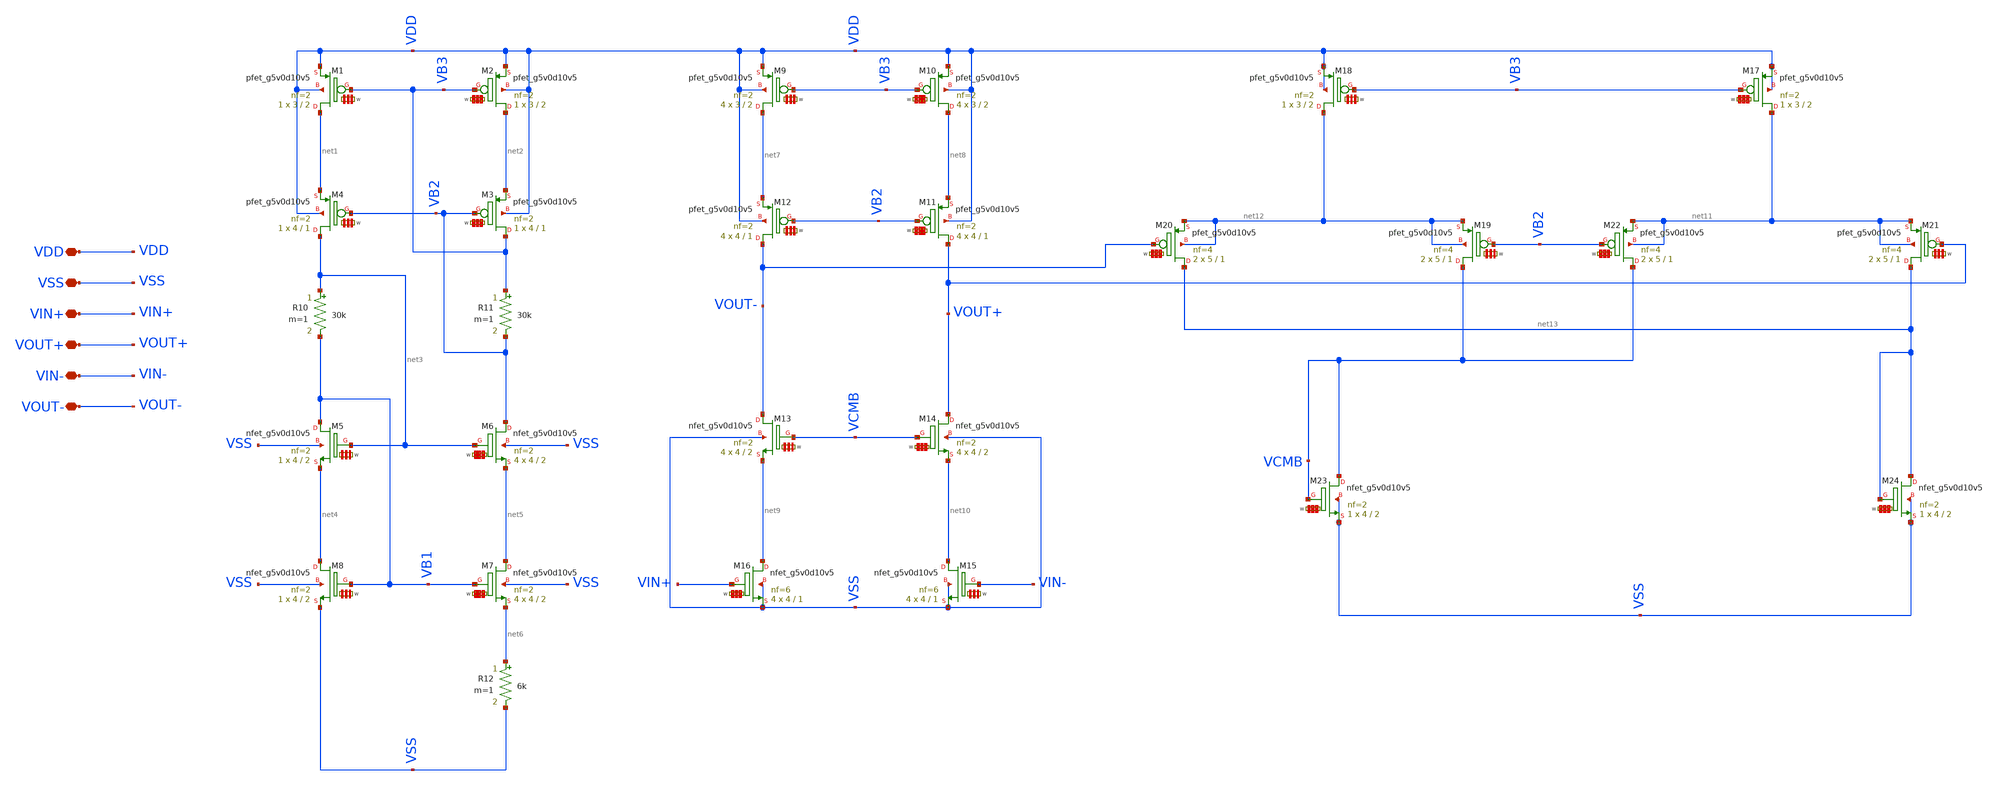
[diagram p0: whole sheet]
** sch_path: my_ip/sky130A/fully_differential_telescopic_cascode_5V_V1/fd_opamp.sch
**.subckt fd_opamp VDD VSS VIN+ VOUT+ VIN- VOUT-
*.iopin VDD
*.iopin VSS
*.iopin VIN+
*.iopin VOUT+
*.iopin VIN-
*.iopin VOUT-
XM1 net1 VB3 VDD VDD sky130_fd_pr__pfet_g5v0d10v5 L=2 W='3 * 2 ' nf=2 ad='int((2 + 1)/2) * 3 * 0.29'
+ as='int((2 + 2)/2) * 3 * 0.29' pd='2*int((2 + 1)/2) * (3 + 0.29)' ps='2*int((2 + 2)/2) * (3 + 0.29)'
+ nrd='0.29 / 3 / 2 ' nrs='0.29 / 3 / 2 ' sa=0 sb=0 sd=0 mult=1 m=1
XM3 VB3 VB2 net2 VDD sky130_fd_pr__pfet_g5v0d10v5 L=1 W='4 * 2 ' nf=2 ad='int((2 + 1)/2) * 4 * 0.29'
+ as='int((2 + 2)/2) * 4 * 0.29' pd='2*int((2 + 1)/2) * (4 + 0.29)' ps='2*int((2 + 2)/2) * (4 + 0.29)'
+ nrd='0.29 / 4 / 2 ' nrs='0.29 / 4 / 2 ' sa=0 sb=0 sd=0 mult=1 m=1
R10 net3 VB1 30k m=1
R11 VB3 VB2 30k m=1
XM7 net5 VB1 net6 VSS sky130_fd_pr__nfet_g5v0d10v5 L=2 W='4 * 2 ' nf=2 ad='int((nf+1)/2) * W / nf * 0.29'
+ as='int((nf+2)/2) * W / nf * 0.29' pd='2*int((nf+1)/2) * (W / nf + 0.29)' ps='2*int((nf+2)/2) * (W / nf + 0.29)'
+ nrd='0.29 / W ' nrs='0.29 / W ' sa=0 sb=0 sd=0 mult=4 m=4
R12 net6 VSS 6k m=1
XM2 net2 VB3 VDD VDD sky130_fd_pr__pfet_g5v0d10v5 L=2 W='3 * 2 ' nf=2 ad='int((2 + 1)/2) * 3 * 0.29'
+ as='int((2 + 2)/2) * 3 * 0.29' pd='2*int((2 + 1)/2) * (3 + 0.29)' ps='2*int((2 + 2)/2) * (3 + 0.29)'
+ nrd='0.29 / 3 / 2 ' nrs='0.29 / 3 / 2 ' sa=0 sb=0 sd=0 mult=1 m=1
XM6 VB2 net3 net5 VSS sky130_fd_pr__nfet_g5v0d10v5 L=2 W='4 * 2 ' nf=2 ad='int((nf+1)/2) * W / nf * 0.29'
+ as='int((nf+2)/2) * W / nf * 0.29' pd='2*int((nf+1)/2) * (W / nf + 0.29)' ps='2*int((nf+2)/2) * (W / nf + 0.29)'
+ nrd='0.29 / W ' nrs='0.29 / W ' sa=0 sb=0 sd=0 mult=4 m=4
XM5 VB1 net3 net4 VSS sky130_fd_pr__nfet_g5v0d10v5 L=2 W='4 * 2 ' nf=2 ad='int((nf+1)/2) * W / nf * 0.29'
+ as='int((nf+2)/2) * W / nf * 0.29' pd='2*int((nf+1)/2) * (W / nf + 0.29)' ps='2*int((nf+2)/2) * (W / nf + 0.29)'
+ nrd='0.29 / W ' nrs='0.29 / W ' sa=0 sb=0 sd=0 mult=1 m=1
XM8 net4 VB1 VSS VSS sky130_fd_pr__nfet_g5v0d10v5 L=2 W='4 * 2 ' nf=2 ad='int((nf+1)/2) * W / nf * 0.29'
+ as='int((nf+2)/2) * W / nf * 0.29' pd='2*int((nf+1)/2) * (W / nf + 0.29)' ps='2*int((nf+2)/2) * (W / nf + 0.29)'
+ nrd='0.29 / W ' nrs='0.29 / W ' sa=0 sb=0 sd=0 mult=1 m=1
XM4 net3 VB2 net1 VDD sky130_fd_pr__pfet_g5v0d10v5 L=1 W='4 * 2 ' nf=2 ad='int((2 + 1)/2) * 4 * 0.29'
+ as='int((2 + 2)/2) * 4 * 0.29' pd='2*int((2 + 1)/2) * (4 + 0.29)' ps='2*int((2 + 2)/2) * (4 + 0.29)'
+ nrd='0.29 / 4 / 2 ' nrs='0.29 / 4 / 2 ' sa=0 sb=0 sd=0 mult=1 m=1
XM9 net7 VB3 VDD VDD sky130_fd_pr__pfet_g5v0d10v5 L=2 W='3 * 2 ' nf=2 ad='int((2 + 1)/2) * 3 * 0.29'
+ as='int((2 + 2)/2) * 3 * 0.29' pd='2*int((2 + 1)/2) * (3 + 0.29)' ps='2*int((2 + 2)/2) * (3 + 0.29)'
+ nrd='0.29 / 3 / 2 ' nrs='0.29 / 3 / 2 ' sa=0 sb=0 sd=0 mult=4 m=4
XM10 net8 VB3 VDD VDD sky130_fd_pr__pfet_g5v0d10v5 L=2 W='3 * 2 ' nf=2 ad='int((2 + 1)/2) * 3 * 0.29'
+ as='int((2 + 2)/2) * 3 * 0.29' pd='2*int((2 + 1)/2) * (3 + 0.29)' ps='2*int((2 + 2)/2) * (3 + 0.29)'
+ nrd='0.29 / 3 / 2 ' nrs='0.29 / 3 / 2 ' sa=0 sb=0 sd=0 mult=4 m=4
XM11 VOUT+ VB2 net8 VDD sky130_fd_pr__pfet_g5v0d10v5 L=1 W='4 * 2 ' nf=2 ad='int((2 + 1)/2) * 4 * 0.29'
+ as='int((2 + 2)/2) * 4 * 0.29' pd='2*int((2 + 1)/2) * (4 + 0.29)' ps='2*int((2 + 2)/2) * (4 + 0.29)'
+ nrd='0.29 / 4 / 2 ' nrs='0.29 / 4 / 2 ' sa=0 sb=0 sd=0 mult=4 m=4
XM12 VOUT- VB2 net7 VDD sky130_fd_pr__pfet_g5v0d10v5 L=1 W='4 * 2 ' nf=2 ad='int((2 + 1)/2) * 4 * 0.29'
+ as='int((2 + 2)/2) * 4 * 0.29' pd='2*int((2 + 1)/2) * (4 + 0.29)' ps='2*int((2 + 2)/2) * (4 + 0.29)'
+ nrd='0.29 / 4 / 2 ' nrs='0.29 / 4 / 2 ' sa=0 sb=0 sd=0 mult=4 m=4
XM15 net10 VIN- VSS VSS sky130_fd_pr__nfet_g5v0d10v5 L=1 W='4 * 6 ' nf=6 ad='int((nf+1)/2) * W / nf * 0.29'
+ as='int((nf+2)/2) * W / nf * 0.29' pd='2*int((nf+1)/2) * (W / nf + 0.29)' ps='2*int((nf+2)/2) * (W / nf + 0.29)'
+ nrd='0.29 / W ' nrs='0.29 / W ' sa=0 sb=0 sd=0 mult=4 m=4
XM17 net11 VB3 VDD VDD sky130_fd_pr__pfet_g5v0d10v5 L=2 W='3 * 2 ' nf=2 ad='int((2 + 1)/2) * 3 * 0.29'
+ as='int((2 + 2)/2) * 3 * 0.29' pd='2*int((2 + 1)/2) * (3 + 0.29)' ps='2*int((2 + 2)/2) * (3 + 0.29)'
+ nrd='0.29 / 3 / 2 ' nrs='0.29 / 3 / 2 ' sa=0 sb=0 sd=0 mult=1 m=1
XM18 net12 VB3 VDD VDD sky130_fd_pr__pfet_g5v0d10v5 L=2 W='3 * 2 ' nf=2 ad='int((2 + 1)/2) * 3 * 0.29'
+ as='int((2 + 2)/2) * 3 * 0.29' pd='2*int((2 + 1)/2) * (3 + 0.29)' ps='2*int((2 + 2)/2) * (3 + 0.29)'
+ nrd='0.29 / 3 / 2 ' nrs='0.29 / 3 / 2 ' sa=0 sb=0 sd=0 mult=1 m=1
XM19 VCMB VB2 net12 net12 sky130_fd_pr__pfet_g5v0d10v5 L=1 W='5 * 4 ' nf=4 ad='int((4 + 1)/2) * 5 * 0.29'
+ as='int((4 + 2)/2) * 5 * 0.29' pd='2*int((4 + 1)/2) * (5 + 0.29)' ps='2*int((4 + 2)/2) * (5 + 0.29)'
+ nrd='0.29 / 5 / 4 ' nrs='0.29 / 5 / 4 ' sa=0 sb=0 sd=0 mult=2 m=2
XM20 net13 VOUT- net12 net12 sky130_fd_pr__pfet_g5v0d10v5 L=1 W='5 * 4 ' nf=4 ad='int((4 + 1)/2) * 5 * 0.29'
+ as='int((4 + 2)/2) * 5 * 0.29' pd='2*int((4 + 1)/2) * (5 + 0.29)' ps='2*int((4 + 2)/2) * (5 + 0.29)'
+ nrd='0.29 / 5 / 4 ' nrs='0.29 / 5 / 4 ' sa=0 sb=0 sd=0 mult=2 m=2
XM21 net13 VOUT+ net11 net11 sky130_fd_pr__pfet_g5v0d10v5 L=1 W='5 * 4 ' nf=4 ad='int((4 + 1)/2) * 5 * 0.29'
+ as='int((4 + 2)/2) * 5 * 0.29' pd='2*int((4 + 1)/2) * (5 + 0.29)' ps='2*int((4 + 2)/2) * (5 + 0.29)'
+ nrd='0.29 / 5 / 4 ' nrs='0.29 / 5 / 4 ' sa=0 sb=0 sd=0 mult=2 m=2
XM22 VCMB VB2 net11 net11 sky130_fd_pr__pfet_g5v0d10v5 L=1 W='5 * 4 ' nf=4 ad='int((4 + 1)/2) * 5 * 0.29'
+ as='int((4 + 2)/2) * 5 * 0.29' pd='2*int((4 + 1)/2) * (5 + 0.29)' ps='2*int((4 + 2)/2) * (5 + 0.29)'
+ nrd='0.29 / 5 / 4 ' nrs='0.29 / 5 / 4 ' sa=0 sb=0 sd=0 mult=2 m=2
XM16 net9 VIN+ VSS VSS sky130_fd_pr__nfet_g5v0d10v5 L=1 W='4 * 6 ' nf=6 ad='int((nf+1)/2) * W / nf * 0.29'
+ as='int((nf+2)/2) * W / nf * 0.29' pd='2*int((nf+1)/2) * (W / nf + 0.29)' ps='2*int((nf+2)/2) * (W / nf + 0.29)'
+ nrd='0.29 / W ' nrs='0.29 / W ' sa=0 sb=0 sd=0 mult=4 m=4
XM13 VOUT- VCMB net9 VSS sky130_fd_pr__nfet_g5v0d10v5 L=2 W='4 * 2 ' nf=2 ad='int((nf+1)/2) * W / nf * 0.29'
+ as='int((nf+2)/2) * W / nf * 0.29' pd='2*int((nf+1)/2) * (W / nf + 0.29)' ps='2*int((nf+2)/2) * (W / nf + 0.29)'
+ nrd='0.29 / W ' nrs='0.29 / W ' sa=0 sb=0 sd=0 mult=4 m=4
XM14 VOUT+ VCMB net10 VSS sky130_fd_pr__nfet_g5v0d10v5 L=2 W='4 * 2 ' nf=2 ad='int((nf+1)/2) * W / nf * 0.29'
+ as='int((nf+2)/2) * W / nf * 0.29' pd='2*int((nf+1)/2) * (W / nf + 0.29)' ps='2*int((nf+2)/2) * (W / nf + 0.29)'
+ nrd='0.29 / W ' nrs='0.29 / W ' sa=0 sb=0 sd=0 mult=4 m=4
XM23 VCMB VCMB VSS VSS sky130_fd_pr__nfet_g5v0d10v5 L=2 W='4 * 2 ' nf=2 ad='int((nf+1)/2) * W / nf * 0.29'
+ as='int((nf+2)/2) * W / nf * 0.29' pd='2*int((nf+1)/2) * (W / nf + 0.29)' ps='2*int((nf+2)/2) * (W / nf + 0.29)'
+ nrd='0.29 / W ' nrs='0.29 / W ' sa=0 sb=0 sd=0 mult=1 m=1
XM24 net13 net13 VSS VSS sky130_fd_pr__nfet_g5v0d10v5 L=2 W='4 * 2 ' nf=2 ad='int((nf+1)/2) * W / nf * 0.29'
+ as='int((nf+2)/2) * W / nf * 0.29' pd='2*int((nf+1)/2) * (W / nf + 0.29)' ps='2*int((nf+2)/2) * (W / nf + 0.29)'
+ nrd='0.29 / W ' nrs='0.29 / W ' sa=0 sb=0 sd=0 mult=1 m=1
**.ends
.end
